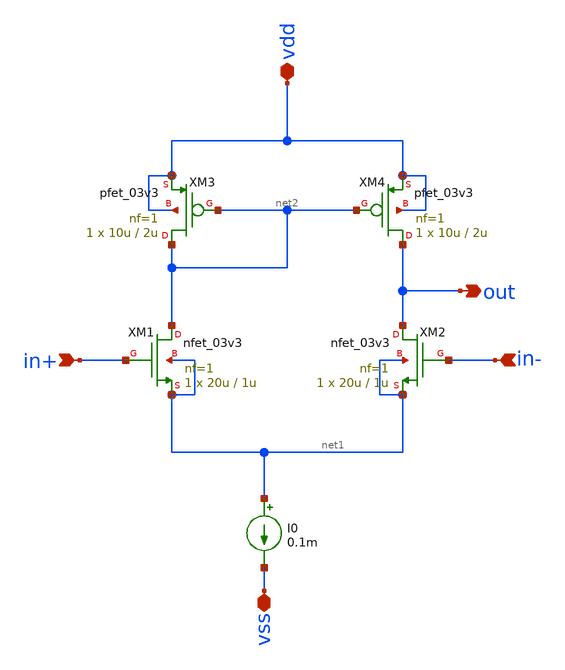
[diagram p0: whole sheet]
** sch_path: Marcel/designs/OP_FS.sch
**.subckt OP_FS out in+ in- vdd vss
*.opin out
*.ipin in+
*.ipin in-
*.iopin vdd
*.iopin vss
XM1 net2 in+ net1 net1 nfet_03v3 L=1u W=20u nf=1 ad='int((nf+1)/2) * W/nf * 0.18u' as='int((nf+2)/2) * W/nf * 0.18u'
+ pd='2*int((nf+1)/2) * (W/nf + 0.18u)' ps='2*int((nf+2)/2) * (W/nf + 0.18u)' nrd='0.18u / W' nrs='0.18u / W'
+ sa=0 sb=0 sd=0 m=1
XM2 out in- net1 net1 nfet_03v3 L=1u W=20u nf=1 ad='int((nf+1)/2) * W/nf * 0.18u' as='int((nf+2)/2) * W/nf * 0.18u'
+ pd='2*int((nf+1)/2) * (W/nf + 0.18u)' ps='2*int((nf+2)/2) * (W/nf + 0.18u)' nrd='0.18u / W' nrs='0.18u / W'
+ sa=0 sb=0 sd=0 m=1
I0 net1 vss 0.1m
XM3 net2 net2 vdd vdd pfet_03v3 L=2u W=10u nf=1 ad='int((nf+1)/2) * W/nf * 0.18u' as='int((nf+2)/2) * W/nf * 0.18u'
+ pd='2*int((nf+1)/2) * (W/nf + 0.18u)' ps='2*int((nf+2)/2) * (W/nf + 0.18u)' nrd='0.18u / W' nrs='0.18u / W'
+ sa=0 sb=0 sd=0 m=1
XM4 out net2 vdd vdd pfet_03v3 L=2u W=10u nf=1 ad='int((nf+1)/2) * W/nf * 0.18u' as='int((nf+2)/2) * W/nf * 0.18u'
+ pd='2*int((nf+1)/2) * (W/nf + 0.18u)' ps='2*int((nf+2)/2) * (W/nf + 0.18u)' nrd='0.18u / W' nrs='0.18u / W'
+ sa=0 sb=0 sd=0 m=1
**.ends
.end
